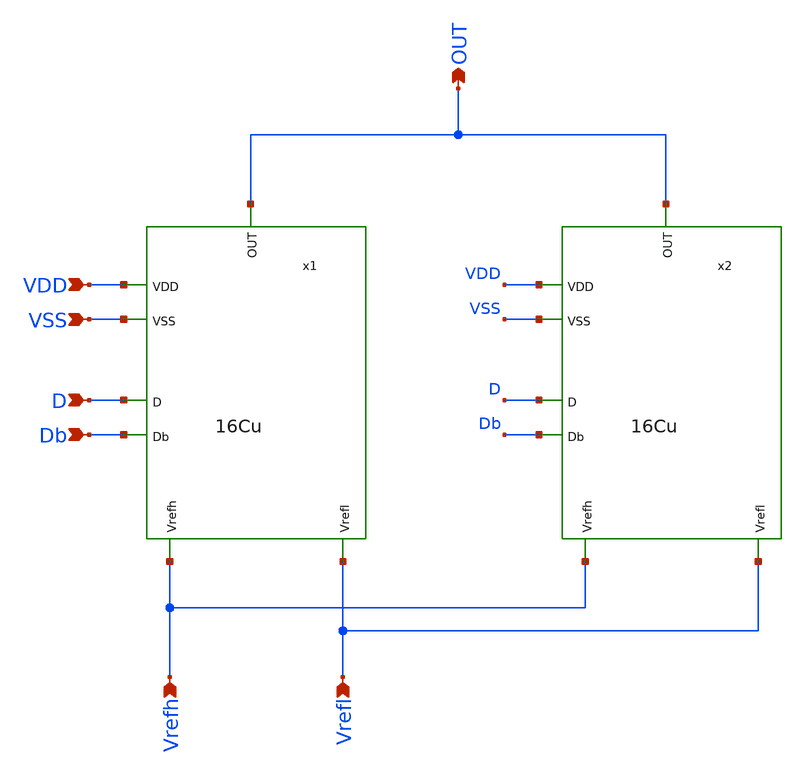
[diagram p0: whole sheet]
** sch_path: 32Cu.sch
**.subckt 32Cu OUT VDD D VSS Vrefh Vrefl Db
*.opin OUT
*.ipin VDD
*.ipin D
*.ipin VSS
*.ipin Vrefh
*.ipin Vrefl
*.ipin Db
x1 OUT VSS VDD Db D Vrefl Vrefh 16Cu
x2 OUT VSS VDD Db D Vrefl Vrefh 16Cu
**.ends
.end
